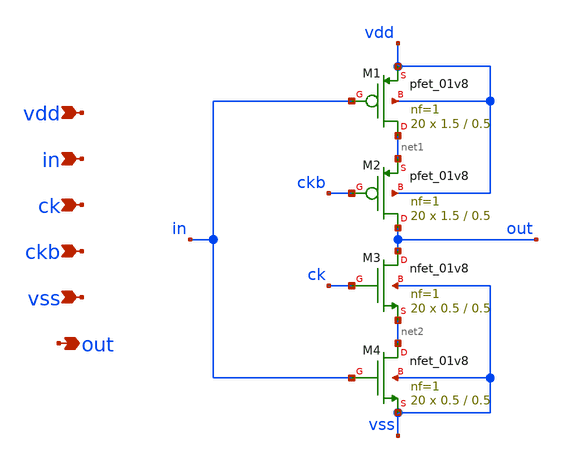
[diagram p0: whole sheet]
** sch_path: xschem/dac_sw_1.sch
**.subckt dac_sw_1 vdd in ck ckb vss out
*.ipin vdd
*.ipin in
*.ipin ck
*.ipin ckb
*.ipin vss
*.opin out
XM1 net1 in vdd vdd sky130_fd_pr__pfet_01v8 L=0.5 W=1.5 nf=1 ad='int((nf+1)/2) * W/nf * 0.29' as='int((nf+2)/2) * W/nf * 0.29'
+ pd='2*int((nf+1)/2) * (W/nf + 0.29)' ps='2*int((nf+2)/2) * (W/nf + 0.29)' nrd='0.29 / W' nrs='0.29 / W'
+ sa=0 sb=0 sd=0 mult=20 m=20
XM2 out ckb net1 vdd sky130_fd_pr__pfet_01v8 L=0.5 W=1.5 nf=1 ad='int((nf+1)/2) * W/nf * 0.29' as='int((nf+2)/2) * W/nf * 0.29'
+ pd='2*int((nf+1)/2) * (W/nf + 0.29)' ps='2*int((nf+2)/2) * (W/nf + 0.29)' nrd='0.29 / W' nrs='0.29 / W'
+ sa=0 sb=0 sd=0 mult=20 m=20
XM3 out ck net2 vss sky130_fd_pr__nfet_01v8 L=0.5 W=0.5 nf=1 ad='int((nf+1)/2) * W/nf * 0.29' as='int((nf+2)/2) * W/nf * 0.29'
+ pd='2*int((nf+1)/2) * (W/nf + 0.29)' ps='2*int((nf+2)/2) * (W/nf + 0.29)' nrd='0.29 / W' nrs='0.29 / W'
+ sa=0 sb=0 sd=0 mult=20 m=20
XM4 net2 in vss vss sky130_fd_pr__nfet_01v8 L=0.5 W=0.5 nf=1 ad='int((nf+1)/2) * W/nf * 0.29' as='int((nf+2)/2) * W/nf * 0.29'
+ pd='2*int((nf+1)/2) * (W/nf + 0.29)' ps='2*int((nf+2)/2) * (W/nf + 0.29)' nrd='0.29 / W' nrs='0.29 / W'
+ sa=0 sb=0 sd=0 mult=20 m=20
**.ends
.end
